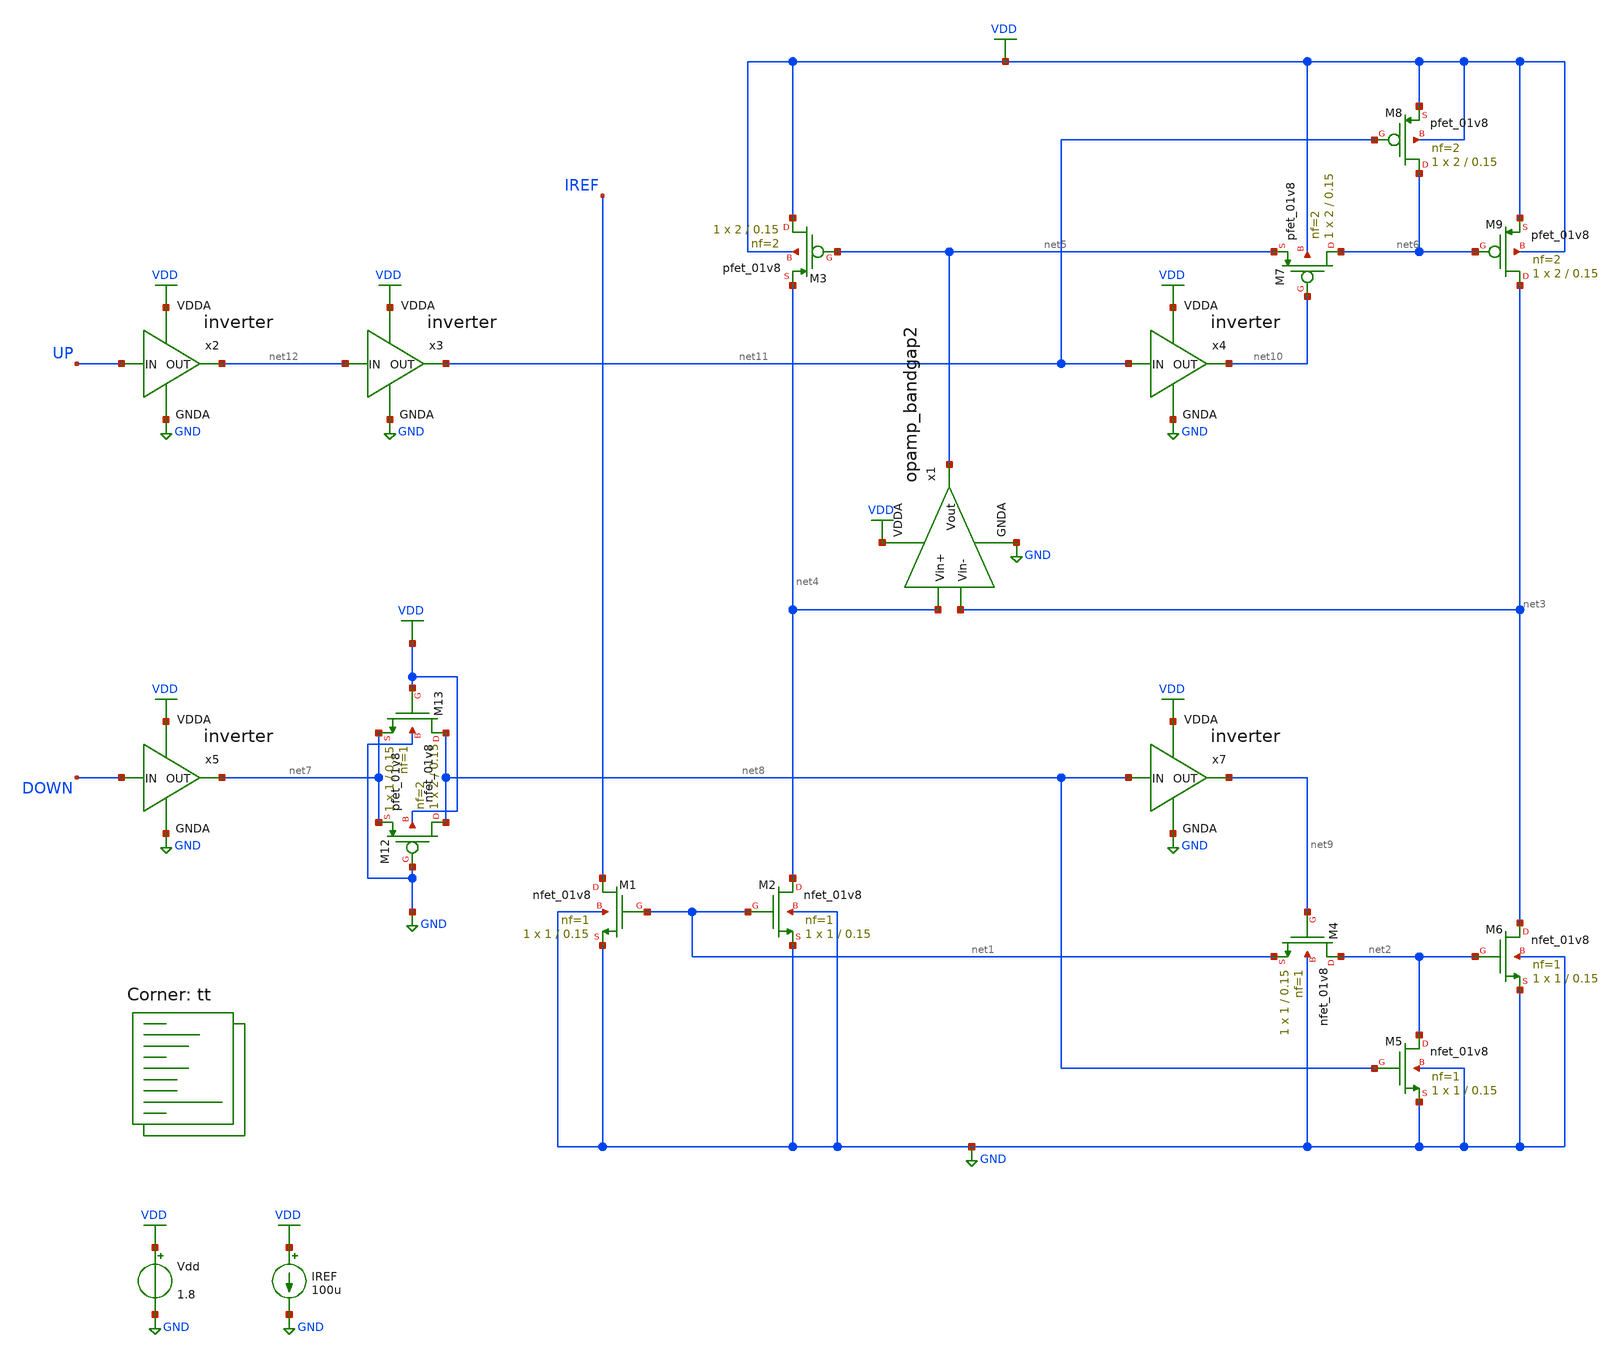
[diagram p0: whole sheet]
** sch_path: projects/pll/charge_pump/xschem_ngspice/charge_pump.sch
**.subckt charge_pump
XM1 IREF net1 GND GND sky130_fd_pr__nfet_01v8 L=0.15 W=1 nf=1 ad='int((nf+1)/2) * W/nf * 0.29' as='int((nf+2)/2) * W/nf * 0.29'
+ pd='2*int((nf+1)/2) * (W/nf + 0.29)' ps='2*int((nf+2)/2) * (W/nf + 0.29)' nrd='0.29 / W' nrs='0.29 / W'
+ sa=0 sb=0 sd=0 mult=1 m=1
XM2 net4 net1 GND GND sky130_fd_pr__nfet_01v8 L=0.15 W=1 nf=1 ad='int((nf+1)/2) * W/nf * 0.29' as='int((nf+2)/2) * W/nf * 0.29'
+ pd='2*int((nf+1)/2) * (W/nf + 0.29)' ps='2*int((nf+2)/2) * (W/nf + 0.29)' nrd='0.29 / W' nrs='0.29 / W'
+ sa=0 sb=0 sd=0 mult=1 m=1
XM4 net2 net9 net1 GND sky130_fd_pr__nfet_01v8 L=0.15 W=1 nf=1 ad='int((nf+1)/2) * W/nf * 0.29' as='int((nf+2)/2) * W/nf * 0.29'
+ pd='2*int((nf+1)/2) * (W/nf + 0.29)' ps='2*int((nf+2)/2) * (W/nf + 0.29)' nrd='0.29 / W' nrs='0.29 / W'
+ sa=0 sb=0 sd=0 mult=1 m=1
XM5 net2 net8 GND GND sky130_fd_pr__nfet_01v8 L=0.15 W=1 nf=1 ad='int((nf+1)/2) * W/nf * 0.29' as='int((nf+2)/2) * W/nf * 0.29'
+ pd='2*int((nf+1)/2) * (W/nf + 0.29)' ps='2*int((nf+2)/2) * (W/nf + 0.29)' nrd='0.29 / W' nrs='0.29 / W'
+ sa=0 sb=0 sd=0 mult=1 m=1
XM6 net3 net2 GND GND sky130_fd_pr__nfet_01v8 L=0.15 W=1 nf=1 ad='int((nf+1)/2) * W/nf * 0.29' as='int((nf+2)/2) * W/nf * 0.29'
+ pd='2*int((nf+1)/2) * (W/nf + 0.29)' ps='2*int((nf+2)/2) * (W/nf + 0.29)' nrd='0.29 / W' nrs='0.29 / W'
+ sa=0 sb=0 sd=0 mult=1 m=1
x1 VDD net5 net3 net4 GND opamp_bandgap2
XM3 VDD net5 net4 VDD sky130_fd_pr__pfet_01v8 L=0.15 W=2 nf=2 ad='int((nf+1)/2) * W/nf * 0.29' as='int((nf+2)/2) * W/nf * 0.29'
+ pd='2*int((nf+1)/2) * (W/nf + 0.29)' ps='2*int((nf+2)/2) * (W/nf + 0.29)' nrd='0.29 / W' nrs='0.29 / W'
+ sa=0 sb=0 sd=0 mult=1 m=1
XM7 net6 net10 net5 VDD sky130_fd_pr__pfet_01v8 L=0.15 W=2 nf=2 ad='int((nf+1)/2) * W/nf * 0.29' as='int((nf+2)/2) * W/nf * 0.29'
+ pd='2*int((nf+1)/2) * (W/nf + 0.29)' ps='2*int((nf+2)/2) * (W/nf + 0.29)' nrd='0.29 / W' nrs='0.29 / W'
+ sa=0 sb=0 sd=0 mult=1 m=1
XM8 net6 net11 VDD VDD sky130_fd_pr__pfet_01v8 L=0.15 W=2 nf=2 ad='int((nf+1)/2) * W/nf * 0.29' as='int((nf+2)/2) * W/nf * 0.29'
+ pd='2*int((nf+1)/2) * (W/nf + 0.29)' ps='2*int((nf+2)/2) * (W/nf + 0.29)' nrd='0.29 / W' nrs='0.29 / W'
+ sa=0 sb=0 sd=0 mult=1 m=1
XM9 net3 net6 VDD VDD sky130_fd_pr__pfet_01v8 L=0.15 W=2 nf=2 ad='int((nf+1)/2) * W/nf * 0.29' as='int((nf+2)/2) * W/nf * 0.29'
+ pd='2*int((nf+1)/2) * (W/nf + 0.29)' ps='2*int((nf+2)/2) * (W/nf + 0.29)' nrd='0.29 / W' nrs='0.29 / W'
+ sa=0 sb=0 sd=0 mult=1 m=1
XM12 net8 GND net7 VDD sky130_fd_pr__pfet_01v8 L=0.15 W=2 nf=2 ad='int((nf+1)/2) * W/nf * 0.29' as='int((nf+2)/2) * W/nf * 0.29'
+ pd='2*int((nf+1)/2) * (W/nf + 0.29)' ps='2*int((nf+2)/2) * (W/nf + 0.29)' nrd='0.29 / W' nrs='0.29 / W'
+ sa=0 sb=0 sd=0 mult=1 m=1
XM13 net8 VDD net7 GND sky130_fd_pr__nfet_01v8 L=0.15 W=1 nf=1 ad='int((nf+1)/2) * W/nf * 0.29' as='int((nf+2)/2) * W/nf * 0.29'
+ pd='2*int((nf+1)/2) * (W/nf + 0.29)' ps='2*int((nf+2)/2) * (W/nf + 0.29)' nrd='0.29 / W' nrs='0.29 / W'
+ sa=0 sb=0 sd=0 mult=1 m=1
x2 VDD net12 UP GND inverter
x3 VDD net11 net12 GND inverter
x4 VDD net10 net11 GND inverter
x5 VDD net7 DOWN GND inverter
x7 VDD net9 net8 GND inverter
IREF VDD GND 100u
Vdd VDD GND 1.8
**** begin user architecture code
.lib $::SKYWATER_MODELS/sky130.lib.spice tt



.option method=gear
.option wnflag=1


.ic v(osc)=0

.temp = 75

.control
  let v_cont_start = 0.6
  let v_cont_stop = 1.9

  dowhile v_cont_start <= v_cont_stop
    alter vcont $&v_cont_start
    save v(osc) v(vcont) v(v1) v(v2) i(vmeas) i(vmeas1)
    tran 1ps 30ns
    remzerovec
    write tb_current_starved_VCO2_{$&v_cont_start}.raw
    linearize v(osc)
    let filename = v_cont_start * 100
    wrdata /foss/designs/my_design/projects/pll/vco/xschem_ngspice/tb_current_starved_VCO2_{$&filename}.txt
+ v(osc)
    set appendwrite

    reset
    let v_cont_start = v_cont_start + 0.1
  end
.endc






**** end user architecture code
**.ends
.GLOBAL VDD
.GLOBAL GND
.end
